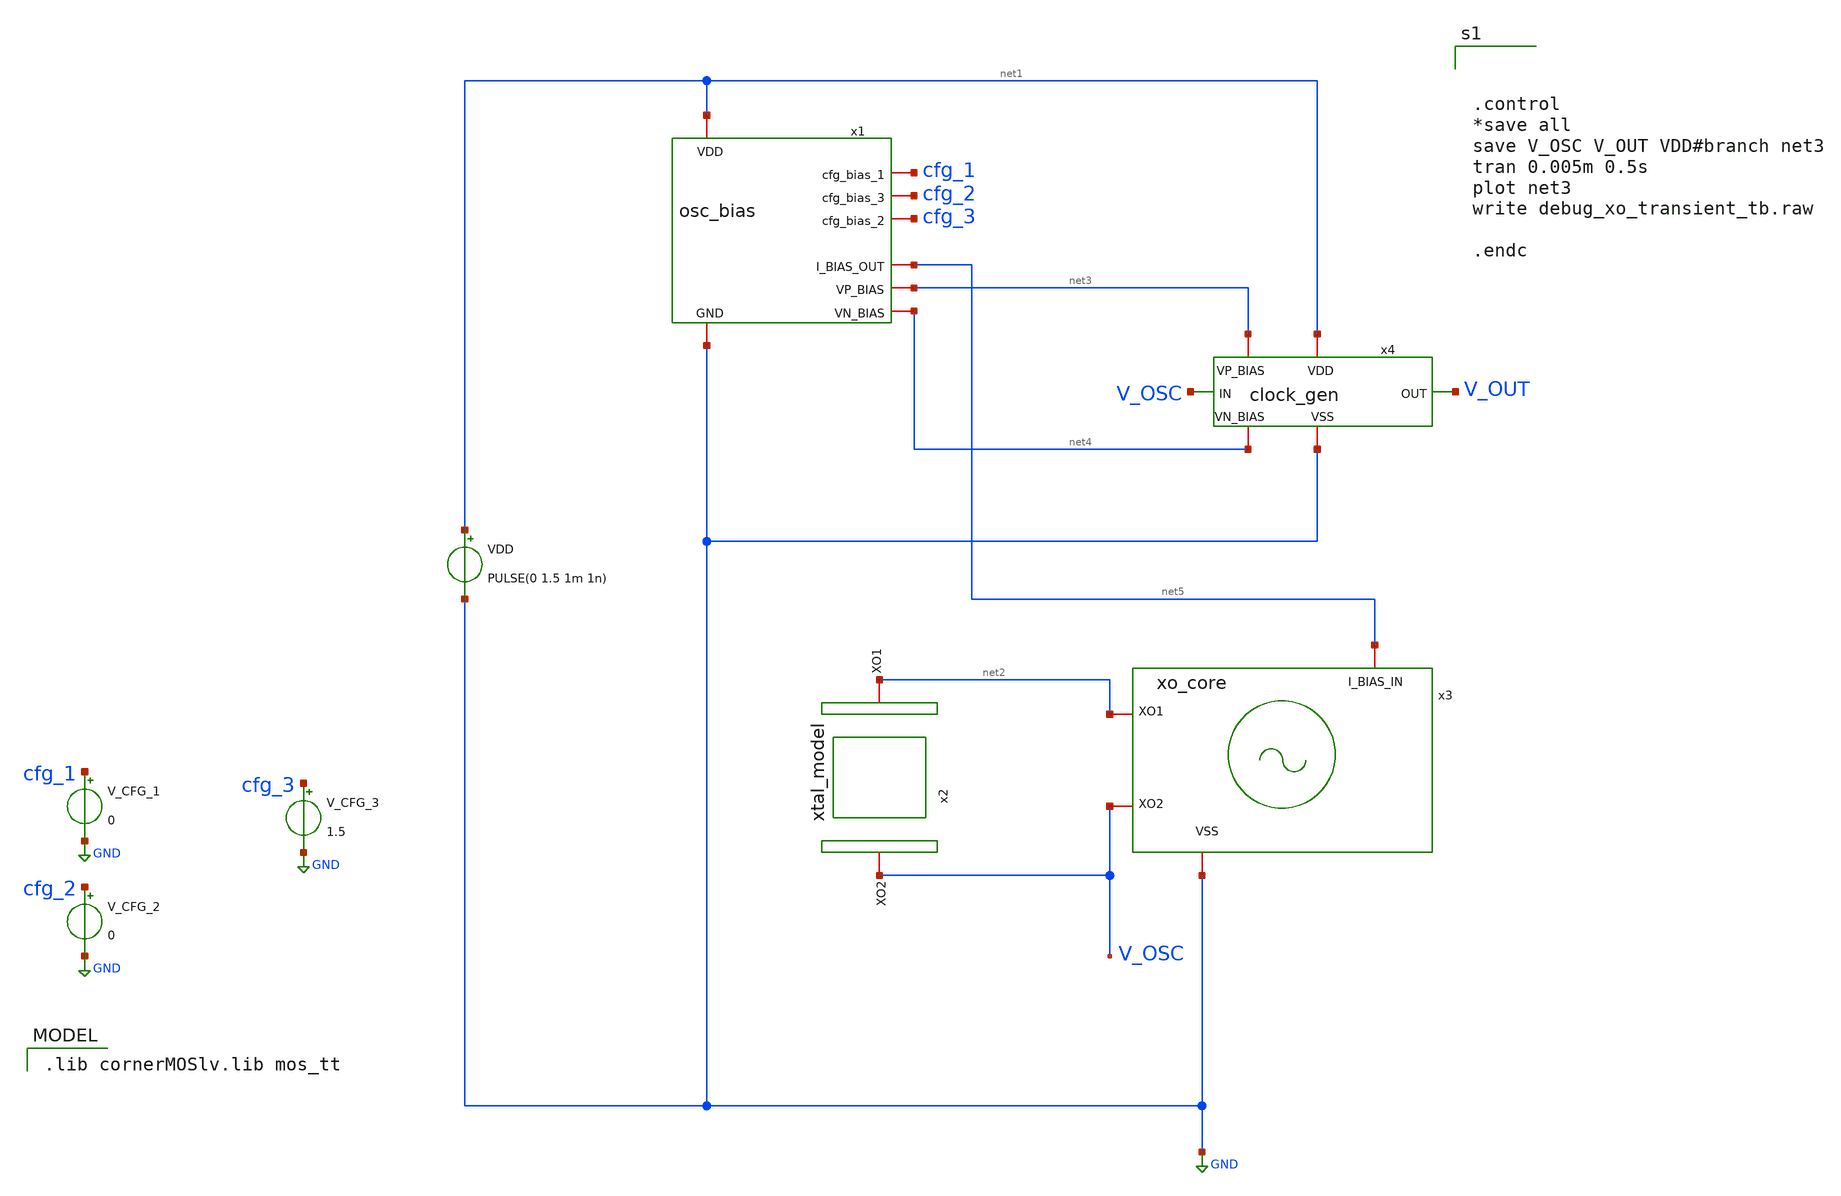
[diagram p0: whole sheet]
** sch_path: debug_xo_transient_tb.sch
**.subckt debug_xo_transient_tb
VDD net1 GND PULSE(0 1.5 1m 1n)
x1 net1 cfg_1 cfg_2 cfg_3 GND net5 net3 net4 osc_bias
x2 net2 V_OSC xtal_model
x3 net5 V_OSC net2 GND xo_core
V_CFG_1 cfg_1 GND 0
V_CFG_2 cfg_2 GND 0
V_CFG_3 cfg_3 GND 1.5
x4 net1 V_OSC V_OUT GND net3 net4 clock_gen
**** begin user architecture code



.control
*save all
save V_OSC V_OUT VDD#branch net3
tran 0.005m 0.5s
plot net3
write debug_xo_transient_tb.raw

.endc


 .lib cornerMOSlv.lib mos_tt

**** end user architecture code
**.ends

* expanding   symbol:  osc_bias.sym # of pins=8
** sym_path: osc_bias.sym
** sch_path: osc_bias.sch
.subckt osc_bias VDD cfg_bias_1 cfg_bias_3 cfg_bias_2 GND I_BIAS_OUT VP_BIAS VN_BIAS
*.iopin VDD
*.iopin GND
*.iopin I_BIAS_OUT
*.iopin cfg_bias_1
*.iopin cfg_bias_2
*.iopin cfg_bias_3
*.opin VN_BIAS
*.opin VP_BIAS
XM1 VP_BIAS VP_BIAS VDD VDD sg13_lv_pmos w=0.25u l=10u ng=1 m=1 mm_ok=1
XM3 VP_BIAS VP_BIAS net1 GND sg13_lv_nmos w=0.25u l=10u ng=1 m=1 mm_ok=1
XM4 net1 net1 net2 GND sg13_lv_nmos w=0.25u l=10u ng=1 m=1 mm_ok=1
XM5 net2 net2 net7 GND sg13_lv_nmos w=0.25u l=10u ng=1 m=1 mm_ok=1
XM2 net6 VP_BIAS VDD VDD sg13_lv_pmos w=2u l=10u ng=1 m=1 mm_ok=1
XM6 I_BIAS_OUT cfg_bias_1 net6 VDD sg13_lv_pmos w=0.25u l=10u ng=1 m=1 mm_ok=1
XM7 net3 VP_BIAS VDD VDD sg13_lv_pmos w=0.5u l=10u ng=1 m=1 mm_ok=1
XM8 net4 VP_BIAS VDD VDD sg13_lv_pmos w=1u l=10u ng=1 m=1 mm_ok=1
XM9 I_BIAS_OUT cfg_bias_2 net3 VDD sg13_lv_pmos w=0.5u l=10u ng=1 m=1 mm_ok=1
XM10 I_BIAS_OUT cfg_bias_3 net4 VDD sg13_lv_pmos w=1u l=10u ng=1 m=1 mm_ok=1
XM11 VN_BIAS VN_BIAS net5 GND sg13_lv_nmos w=0.25u l=10u ng=1 m=1 mm_ok=1
Vmeas net5 GND 0
.save i(vmeas)
C1 VDD VP_BIAS 1p m=1
R1 VDD VP_BIAS 100Meg m=1
XM12 net7 net7 VN_BIAS GND sg13_lv_nmos w=0.25u l=10u ng=1 m=1 mm_ok=1
.ends


* expanding   symbol:  xtal_model.sym # of pins=2
** sym_path: xtal_model.sym
** sch_path: xtal_model.sch
.subckt xtal_model XO1 XO2
*.iopin XO2
*.iopin XO1
R1 XO1 net1 1k m=1
Cm net1 net2 1p m=1
C0 XO1 XO2 1p m=1
Lm net2 XO2 1n m=1
.ends


* expanding   symbol:  xo_core.sym # of pins=4
** sym_path: xo_core.sym
** sch_path: xo_core.sch
.subckt xo_core I_BIAS_IN XO2 XO1 VSS
*.iopin VSS
*.ipin I_BIAS_IN
*.iopin XO1
*.iopin XO2
XM2 net1 XO1 XO1 XO1 sg13_lv_pmos w=2u l=2u ng=1 m=1 mm_ok=1
XM3 XO2 net1 net1 net1 sg13_lv_pmos w=2u l=2u ng=1 m=1 mm_ok=1
XM1 XO2 XO1 VSS VSS sg13_lv_nmos w=1.0u l=1.0u ng=1 m=1 mm_ok=1
C2 XO2 VSS 8p m=1
C1 XO1 VSS 8p m=1
Vmeas I_BIAS_IN XO2 0
.save i(vmeas)
.ends


* expanding   symbol:  clock_gen.sym # of pins=6
** sym_path: clock_gen.sym
** sch_path: clock_gen.sch
.subckt clock_gen VDD IN OUT VSS VP_BIAS VN_BIAS
*.iopin VSS
*.iopin VDD
*.ipin IN
*.opin OUT
*.ipin VP_BIAS
*.ipin VN_BIAS
XM1 stage_1 net1 net3 VSS sg13_lv_nmos w=1u l=0.13u ng=1 m=1 mm_ok=1
XM2 stage_1 net1 net2 VDD sg13_lv_pmos w=1u l=0.13u ng=1 m=1 mm_ok=1
R1 stage_1 net1 100Meg m=1
C1 IN net1 200p m=1
XM3 stage_2 stage_1 net5 VSS sg13_lv_nmos w=3u l=0.13u ng=1 m=1 mm_ok=1
XM4 stage_2 stage_1 net4 VDD sg13_lv_pmos w=6u l=0.13u ng=1 m=1 mm_ok=1
XM5 OUT stage_2 net7 VSS sg13_lv_nmos w=4.5u l=0.13u ng=1 m=1 mm_ok=1
XM6 OUT stage_2 net6 VDD sg13_lv_pmos w=9u l=0.13u ng=1 m=1 mm_ok=1
XM7 net2 VP_BIAS net9 VDD sg13_lv_pmos w=1.8u l=10u ng=1 m=1 mm_ok=1
XM8 net3 VN_BIAS net8 VSS sg13_lv_nmos w=0.9u l=10u ng=1 m=1 mm_ok=1
XM9 net4 VP_BIAS VDD VDD sg13_lv_pmos w=3.6u l=10u ng=1 m=1 mm_ok=1
XM10 net5 VN_BIAS VSS VSS sg13_lv_nmos w=1.8u l=10u ng=1 m=1 mm_ok=1
XM11 net6 VP_BIAS VDD VDD sg13_lv_pmos w=1.8u l=10u ng=1 m=1 mm_ok=1
XM12 net7 VN_BIAS VSS VSS sg13_lv_nmos w=0.9u l=10u ng=1 m=1 mm_ok=1
Vmeas_NMOS net8 VSS 0
.save i(vmeas_nmos)
Vmeas_PMOS VDD net9 0
.save i(vmeas_pmos)
.ends

.GLOBAL GND
.end
